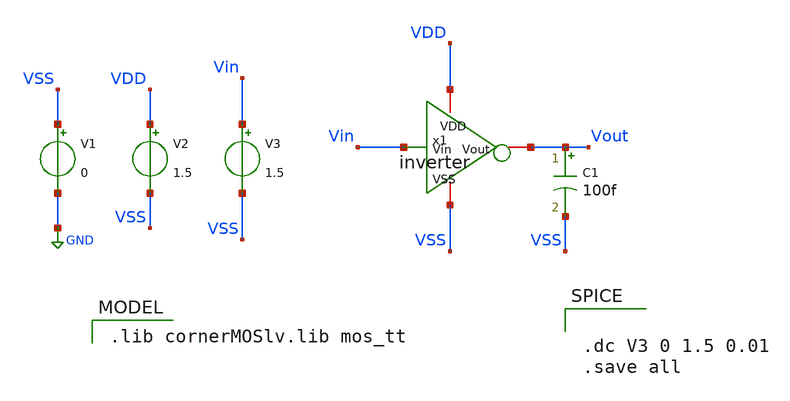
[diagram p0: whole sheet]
** sch_path: inverter_tutorial/xschem/inverter_tb.sch
**.subckt inverter_tb
C1 Vout VSS 100f m=1
V1 VSS GND 0
V2 VDD VSS 1.5
V3 Vin VSS 1.5
x1 VDD Vout Vin VSS inverter
**** begin user architecture code
 .lib cornerMOSlv.lib mos_tt



.dc V3 0 1.5 0.01
.save all


**** end user architecture code
**.ends

* expanding   symbol:  /home/edney_freitas/Tutorial/inverter_tutorial/xschem/inverter.sym # of
*+ pins=4
** sym_path: inverter_tutorial/xschem/inverter.sym
** sch_path: inverter_tutorial/xschem/inverter.sch
.subckt inverter VDD Vout Vin VSS
*.ipin Vin
*.iopin VDD
*.iopin Vout
*.iopin VSS
XM1 Vout Vin VSS VSS sg13_lv_nmos w=1u l=0.13u ng=1 m=1 mm_ok=1
XM2 Vout Vin VDD VDD sg13_lv_pmos w=3u l=0.13u ng=1 m=1 mm_ok=1
.ends

.GLOBAL GND
.end
